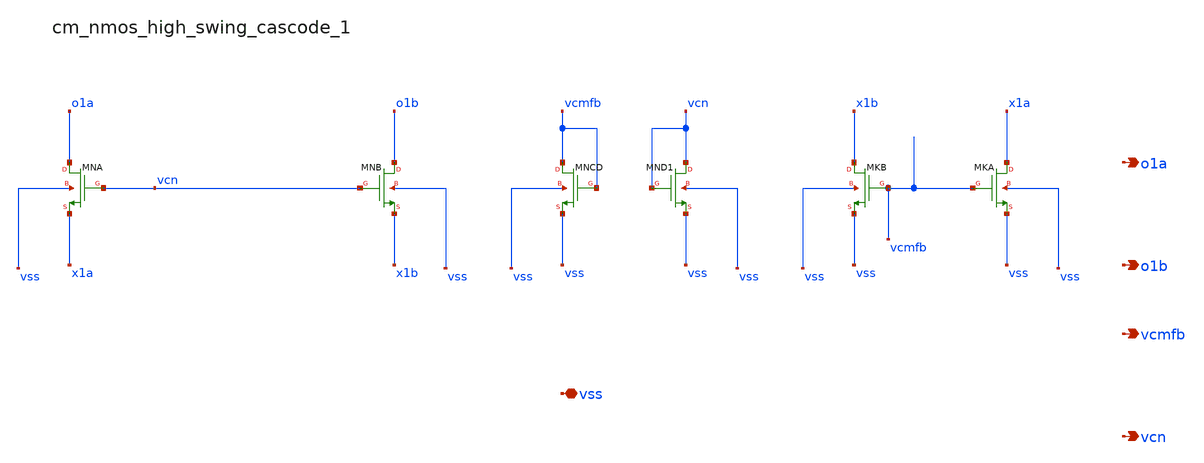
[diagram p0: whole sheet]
** sch_path: analog-db/raw/amp_023_fer_fd2s/hier/blocks/cm_nmos_high_swing_cascode_1.sch
**.subckt cm_nmos_high_swing_cascode_1 vss o1a o1b vcmfb vcn
*.iopin vss
*.opin o1a
*.opin o1b
*.opin vcmfb
*.opin vcn
XMKA x1a vcmfb vss vss sg13_lv_nmos w=x_dut_xmka_w l=x_dut_xmka_l ng=1 m=x_dut_xmka_m
XMKB x1b vcmfb vss vss sg13_lv_nmos w=x_dut_xmkb_w l=x_dut_xmkb_l ng=1 m=x_dut_xmkb_m
XMNA o1a vcn x1a vss sg13_lv_nmos w=x_dut_xmna_w l=x_dut_xmna_l ng=1 m=x_dut_xmna_m
XMNB o1b vcn x1b vss sg13_lv_nmos w=x_dut_xmnb_w l=x_dut_xmnb_l ng=1 m=x_dut_xmnb_m
XMNCD vcmfb vcmfb vss vss sg13_lv_nmos w=x_dut_xmncd_w l=x_dut_xmncd_l ng=1 m=x_dut_xmncd_m
XMND1 vcn vcn vss vss sg13_lv_nmos w=x_dut_xmnd1_w l=x_dut_xmnd1_l ng=1 m=x_dut_xmnd1_m
**.ends
.end
